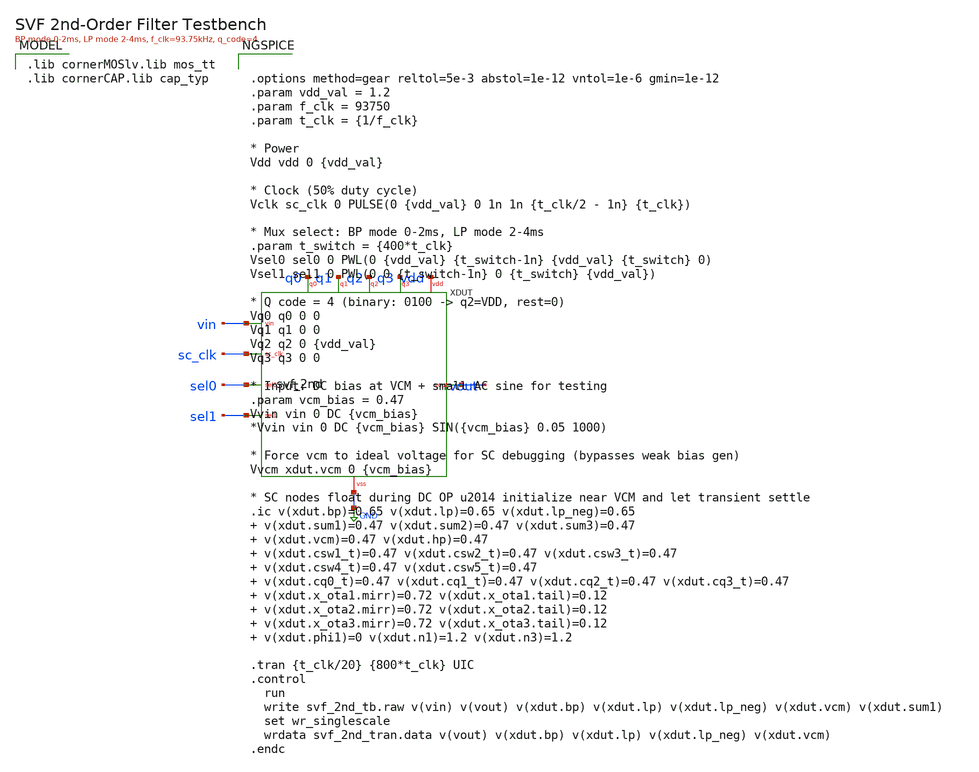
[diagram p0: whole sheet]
** sch_path: xschem/svf_2nd_tb.sch
**.subckt svf_2nd_tb
XDUT vin vout sc_clk sel0 sel1 q0 q1 q2 q3 vdd GND svf_2nd
**** begin user architecture code
 .lib cornerMOSlv.lib mos_tt
.lib cornerCAP.lib cap_typ



.options method=gear reltol=5e-3 abstol=1e-12 vntol=1e-6 gmin=1e-12
.param vdd_val = 1.2
.param f_clk = 93750
.param t_clk = {1/f_clk}

* Power
Vdd vdd 0 {vdd_val}

* Clock (50% duty cycle)
Vclk sc_clk 0 PULSE(0 {vdd_val} 0 1n 1n {t_clk/2 - 1n} {t_clk})

* Mux select: BP mode 0-2ms, LP mode 2-4ms
.param t_switch = {400*t_clk}
Vsel0 sel0 0 PWL(0 {vdd_val} {t_switch-1n} {vdd_val} {t_switch} 0)
Vsel1 sel1 0 PWL(0 0 {t_switch-1n} 0 {t_switch} {vdd_val})

* Q code = 4 (binary: 0100 -> q2=VDD, rest=0)
Vq0 q0 0 0
Vq1 q1 0 0
Vq2 q2 0 {vdd_val}
Vq3 q3 0 0

* Input: DC bias at VCM + small AC sine for testing
.param vcm_bias = 0.47
Vvin vin 0 DC {vcm_bias}
*Vvin vin 0 DC {vcm_bias} SIN({vcm_bias} 0.05 1000)

* Force vcm to ideal voltage for SC debugging (bypasses weak bias gen)
Vvcm xdut.vcm 0 {vcm_bias}

* SC nodes float during DC OP u2014 initialize near VCM and let transient settle
.ic v(xdut.bp)=0.65 v(xdut.lp)=0.65 v(xdut.lp_neg)=0.65  v(xdut.sum1)=0.47 v(xdut.sum2)=0.47
+ v(xdut.sum3)=0.47  v(xdut.vcm)=0.47 v(xdut.hp)=0.47  v(xdut.csw1_t)=0.47 v(xdut.csw2_t)=0.47 v(xdut.csw3_t)=0.47
+  v(xdut.csw4_t)=0.47 v(xdut.csw5_t)=0.47  v(xdut.cq0_t)=0.47 v(xdut.cq1_t)=0.47 v(xdut.cq2_t)=0.47 v(xdut.cq3_t)=0.47
+  v(xdut.x_ota1.mirr)=0.72 v(xdut.x_ota1.tail)=0.12  v(xdut.x_ota2.mirr)=0.72 v(xdut.x_ota2.tail)=0.12
+  v(xdut.x_ota3.mirr)=0.72 v(xdut.x_ota3.tail)=0.12  v(xdut.phi1)=0 v(xdut.n1)=1.2 v(xdut.n3)=1.2

.tran {t_clk/20} {800*t_clk} UIC
.control
  run
  write svf_2nd_tb.raw v(vin) v(vout) v(xdut.bp) v(xdut.lp) v(xdut.lp_neg) v(xdut.vcm) v(xdut.sum1)
  set wr_singlescale
  wrdata svf_2nd_tran.data v(vout) v(xdut.bp) v(xdut.lp) v(xdut.lp_neg) v(xdut.vcm)
.endc


**** end user architecture code
**.ends

* expanding   symbol:  svf_2nd.sym # of pins=11
** sym_path: xschem/svf_2nd.sym
** sch_path: xschem/svf_2nd.sch
.subckt svf_2nd vin vout sc_clk sel0 sel1 q0 q1 q2 q3 vdd vss
*.ipin vin
*.opin vout
*.ipin sc_clk
*.ipin sel0
*.ipin sel1
*.ipin q0
*.ipin q1
*.ipin q2
*.ipin q3
*.iopin vdd
*.iopin vss
XXXMPbias vcm vcm vdd vdd sg13_lv_pmos w=2e-6 l=0.5e-6 ng=1 m=1 mm_ok=1
XXXMNbias vcm vcm vss vss sg13_lv_nmos w=2e-6 l=0.5e-6 ng=1 m=1 mm_ok=1
XXXMP_n0 n1 sc_clk vdd vdd sg13_lv_pmos w=2e-6 l=0.13e-6 ng=1 m=1 mm_ok=1
XXXMN_n0 n1 sc_clk vss vss sg13_lv_nmos w=1e-6 l=0.13e-6 ng=1 m=1 mm_ok=1
XXXMP_n1 phi1 n1 vdd vdd sg13_lv_pmos w=2e-6 l=0.13e-6 ng=1 m=1 mm_ok=1
XXXMN_n1 phi1 n1 vss vss sg13_lv_nmos w=1e-6 l=0.13e-6 ng=1 m=1 mm_ok=1
XXXMP_n2 n3 phi1 vdd vdd sg13_lv_pmos w=2e-6 l=0.13e-6 ng=1 m=1 mm_ok=1
XXXMN_n2 n3 phi1 vss vss sg13_lv_nmos w=1e-6 l=0.13e-6 ng=1 m=1 mm_ok=1
x_sw0_in vin csw1_t phi1 n3 vss vdd cmos_tg
x_sw0_ref vcm csw1_t n3 phi1 vss vdd cmos_tg
XXC_sw1 csw1_t sum1 cap_cmim w=7.0e-6 l=7.0e-6 m=1 mm_ok=1
x_sw2_in lp csw2_t phi1 n3 vss vdd cmos_tg
x_sw2_ref vcm csw2_t n3 phi1 vss vdd cmos_tg
XXC_sw2 csw2_t sum1 cap_cmim w=7.0e-6 l=7.0e-6 m=1 mm_ok=1
XXC_int1 bp sum1 cap_cmim w=23.1e-6 l=23.1e-6 m=1 mm_ok=1
x_ota1 vcm sum1 vcm bp vdd vss svf_ota5t
x_sw6_in bp csw3_t phi1 n3 vss vdd cmos_tg
x_sw6_ref vcm csw3_t n3 phi1 vss vdd cmos_tg
XXC_sw3 csw3_t sum2 cap_cmim w=7.0e-6 l=7.0e-6 m=1 mm_ok=1
XXC_int2 lp_neg sum2 cap_cmim w=23.1e-6 l=23.1e-6 m=1 mm_ok=1
x_ota2 vcm sum2 vcm lp_neg vdd vss svf_ota5t
x_sw8_in lp_neg csw4_t phi1 n3 vss vdd cmos_tg
x_sw8_ref vcm csw4_t n3 phi1 vss vdd cmos_tg
XXC_sw4 csw4_t sum3 cap_cmim w=7.0e-6 l=7.0e-6 m=1 mm_ok=1
x_sw10_in lp csw5_t phi1 n3 vss vdd cmos_tg
x_sw10_ref vcm csw5_t n3 phi1 vss vdd cmos_tg
XXC_sw5 csw5_t sum3 cap_cmim w=7.0e-6 l=7.0e-6 m=1 mm_ok=1
XXC_int3 lp sum3 cap_cmim w=23.1e-6 l=23.1e-6 m=1 mm_ok=1
x_ota3 vcm sum3 vcm lp vdd vss svf_ota5t
x_swq0_en bp net1 q0 q0_b vss vdd cmos_tg
x_swq0_phi net1 cq0_t phi1 n3 vss vdd cmos_tg
x_swq0_ref vcm cq0_t n3 phi1 vss vdd cmos_tg
XXC_q0 cq0_t sum1 cap_cmim w=1.81e-6 l=1.81e-6 m=1 mm_ok=1
x_swq1_en bp net2 q1 q1_b vss vdd cmos_tg
x_swq1_phi net2 cq1_t phi1 n3 vss vdd cmos_tg
x_swq1_ref vcm cq1_t n3 phi1 vss vdd cmos_tg
XXC_q1 cq1_t sum1 cap_cmim w=2.56e-6 l=2.56e-6 m=1 mm_ok=1
x_swq2_en bp net3 q2 q2_b vss vdd cmos_tg
x_swq2_phi net3 cq2_t phi1 n3 vss vdd cmos_tg
x_swq2_ref vcm cq2_t n3 phi1 vss vdd cmos_tg
XXC_q2 cq2_t sum1 cap_cmim w=3.62e-6 l=3.62e-6 m=1 mm_ok=1
x_swq3_en bp net4 q3 q3_b vss vdd cmos_tg
x_swq3_phi net4 cq3_t phi1 n3 vss vdd cmos_tg
x_swq3_ref vcm cq3_t n3 phi1 vss vdd cmos_tg
XXC_q3 cq3_t sum1 cap_cmim w=5.11e-6 l=5.11e-6 m=1 mm_ok=1
x_mux_lp lp vout sel1 sel1_b vss vdd cmos_tg
x_mux_bp bp vout sel0 sel0_b vss vdd cmos_tg
x_mux_hp hp vout vss vdd vss vdd cmos_tg
x_mux_byp vin vout vss vdd vss vdd cmos_tg
XXXMP_invq0 q0_b q0 vdd vdd sg13_lv_pmos w=2e-6 l=0.13e-6 ng=1 m=1 mm_ok=1
XXXMN_invq0 q0_b q0 vss vss sg13_lv_nmos w=1e-6 l=0.13e-6 ng=1 m=1 mm_ok=1
XXXMP_invq1 q1_b q1 vdd vdd sg13_lv_pmos w=2e-6 l=0.13e-6 ng=1 m=1 mm_ok=1
XXXMN_invq1 q1_b q1 vss vss sg13_lv_nmos w=1e-6 l=0.13e-6 ng=1 m=1 mm_ok=1
XXXMP_invq2 q2_b q2 vdd vdd sg13_lv_pmos w=2e-6 l=0.13e-6 ng=1 m=1 mm_ok=1
XXXMN_invq2 q2_b q2 vss vss sg13_lv_nmos w=1e-6 l=0.13e-6 ng=1 m=1 mm_ok=1
XXXMP_invq3 q3_b q3 vdd vdd sg13_lv_pmos w=2e-6 l=0.13e-6 ng=1 m=1 mm_ok=1
XXXMN_invq3 q3_b q3 vss vss sg13_lv_nmos w=1e-6 l=0.13e-6 ng=1 m=1 mm_ok=1
XXXMP_invs0 sel0_b sel0 vdd vdd sg13_lv_pmos w=2e-6 l=0.13e-6 ng=1 m=1 mm_ok=1
XXXMN_invs0 sel0_b sel0 vss vss sg13_lv_nmos w=1e-6 l=0.13e-6 ng=1 m=1 mm_ok=1
XXXMP_invs1 sel1_b sel1 vdd vdd sg13_lv_pmos w=2e-6 l=0.13e-6 ng=1 m=1 mm_ok=1
XXXMN_invs1 sel1_b sel1 vss vss sg13_lv_nmos w=1e-6 l=0.13e-6 ng=1 m=1 mm_ok=1
.ends


* expanding   symbol:  cmos_tg.sym # of pins=6
** sym_path: xschem/cmos_tg.sym
** sch_path: xschem/cmos_tg.sch
.subckt cmos_tg a b ctrl_n ctrl_p vss vdd
*.iopin a
*.iopin b
*.ipin ctrl_p
*.iopin vss
*.iopin vdd
*.ipin ctrl_n
XXMN a ctrl_n b vss sg13_lv_nmos w=2e-6 l=0.13e-6 ng=1 m=1 mm_ok=1
XXMP b ctrl_p a vdd sg13_lv_pmos w=4e-6 l=0.13e-6 ng=1 m=1 mm_ok=1
.ends


* expanding   symbol:  svf_ota5t.sym # of pins=6
** sym_path: xschem/svf_ota5t.sym
** sch_path: xschem/svf_ota5t.sch
.subckt svf_ota5t vinp vinn vbias vout vdd vss
*.iopin vdd
*.iopin vss
*.ipin vinp
*.ipin vinn
*.opin vout
*.ipin vbias
XXM3 mirr mirr vdd vdd sg13_lv_pmos w=2e-6 l=0.5e-6 ng=1 m=1 mm_ok=1
XXM4 vout mirr vdd vdd sg13_lv_pmos w=2e-6 l=0.5e-6 ng=1 m=1 mm_ok=1
XXM1 mirr vinp tail vss sg13_lv_nmos w=4e-6 l=0.5e-6 ng=1 m=1 mm_ok=1
XXM2 vout vinn tail vss sg13_lv_nmos w=4e-6 l=0.5e-6 ng=1 m=1 mm_ok=1
XXM5 tail vbias vss vss sg13_lv_nmos w=2e-6 l=0.5e-6 ng=1 m=1 mm_ok=1
.ends

.GLOBAL GND
.end
